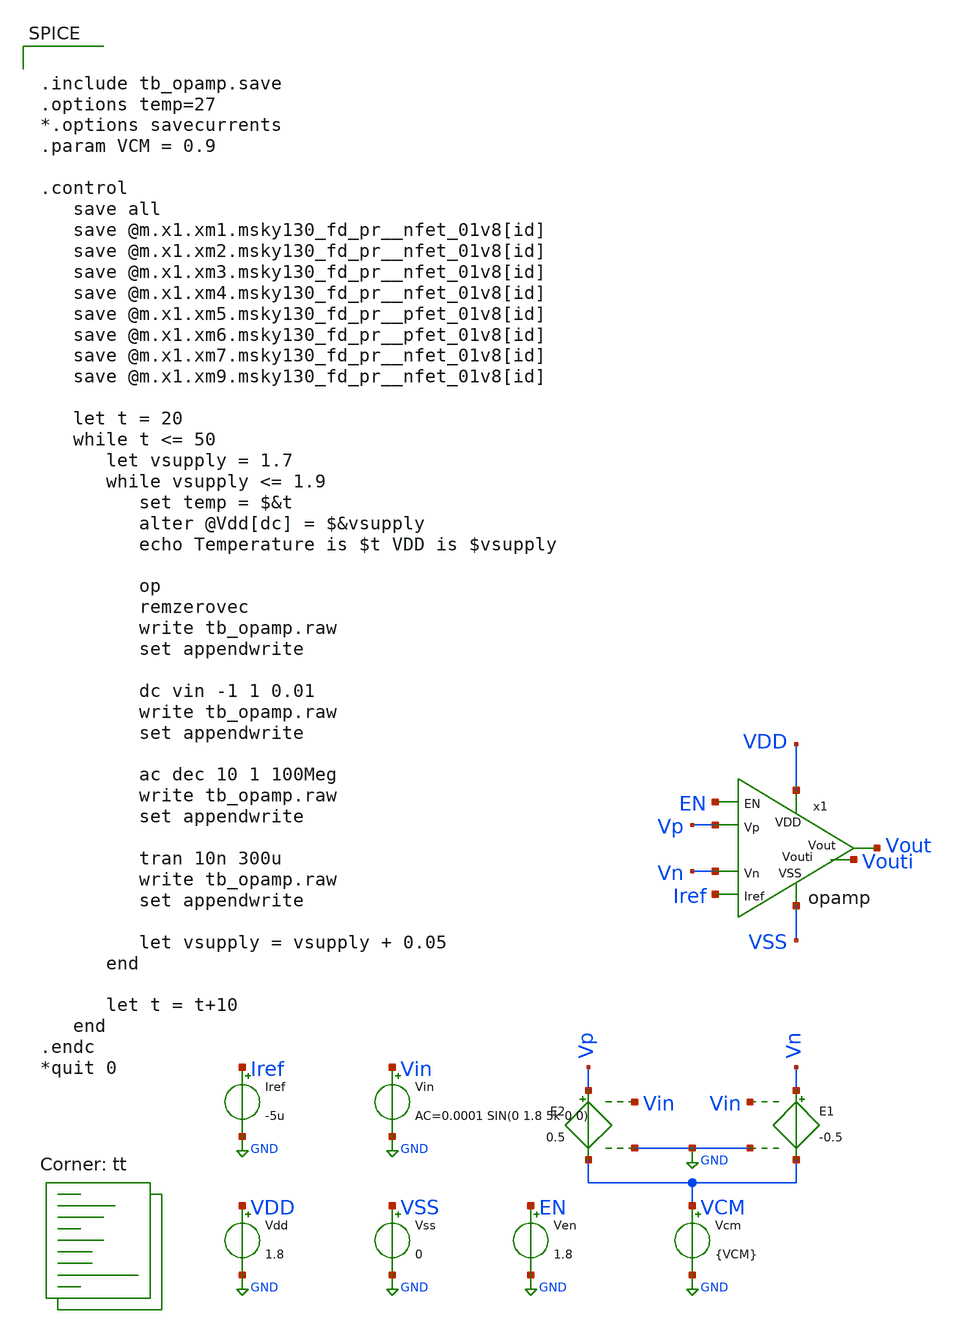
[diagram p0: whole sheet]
** sch_path: xschem/tb_opamp.sch
**.subckt tb_opamp
Vdd VDD GND 1.8
Vss VSS GND 0
E1 Vn VCM Vin GND -0.5
Vcm VCM GND {VCM}
E2 Vp VCM Vin GND 0.5
Vin Vin GND AC=0.0001 SIN(0 1.8 5k 0 0)
Iref Iref GND -5u
x1 Vout Vn Vp VSS Iref VDD Vouti EN opamp
Ven EN GND 1.8
**** begin user architecture code


.include tb_opamp.save
.options temp=27
*.options savecurrents
.param VCM = 0.9

.control
   save all
   save @m.x1.xm1.msky130_fd_pr__nfet_01v8[id]
   save @m.x1.xm2.msky130_fd_pr__nfet_01v8[id]
   save @m.x1.xm3.msky130_fd_pr__nfet_01v8[id]
   save @m.x1.xm4.msky130_fd_pr__nfet_01v8[id]
   save @m.x1.xm5.msky130_fd_pr__pfet_01v8[id]
   save @m.x1.xm6.msky130_fd_pr__pfet_01v8[id]
   save @m.x1.xm7.msky130_fd_pr__nfet_01v8[id]
   save @m.x1.xm9.msky130_fd_pr__nfet_01v8[id]

   let t = 20
   while t <= 50
      let vsupply = 1.7
      while vsupply <= 1.9
         set temp = $&t
         alter @Vdd[dc] = $&vsupply
         echo Temperature is $t VDD is $vsupply

         op
         remzerovec
         write tb_opamp.raw
         set appendwrite

         dc vin -1 1 0.01
         write tb_opamp.raw
         set appendwrite

         ac dec 10 1 100Meg
         write tb_opamp.raw
         set appendwrite

         tran 10n 300u
         write tb_opamp.raw
         set appendwrite

         let vsupply = vsupply + 0.05
      end

      let t = t+10
   end
.endc
*quit 0


.lib $::SKYWATER_MODELS/sky130.lib.spice tt
**** end user architecture code
**.ends

* expanding   symbol:  /foss/designs/ttsky_opamp/xschem/opamp.sym # of pins=8
** sym_path: xschem/opamp.sym
** sch_path: xschem/opamp.sch
.subckt opamp Vout Vn Vp VSS Iref VDD Vouti EN
*.ipin VSS
*.ipin Vp
*.opin Vout
*.ipin Vn
*.ipin VDD
*.ipin Iref
*.opin Vouti
*.ipin EN
XM1 VGref VGref VSS VSS sky130_fd_pr__nfet_01v8 L=1 W=4 nf=1 ad='int((1 + 1)/2) * 4 / 1 * 0.29' as='int((1 + 2)/2) * 4 / 1 * 0.29'
+ pd='2*int((1 + 1)/2) * (4 / 1 + 0.29)' ps='2*int((1 + 2)/2) * (4 / 1 + 0.29)' nrd='0.29 / 4 ' nrs='0.29 / 4 '
+ sa=0 sb=0 sd=0 mult=1 m=1
XM2 Vx VGref VSS VSS sky130_fd_pr__nfet_01v8 L=1 W=4 nf=1 ad='int((1 + 1)/2) * 4 / 1 * 0.29' as='int((1 + 2)/2) * 4 / 1 * 0.29'
+ pd='2*int((1 + 1)/2) * (4 / 1 + 0.29)' ps='2*int((1 + 2)/2) * (4 / 1 + 0.29)' nrd='0.29 / 4 ' nrs='0.29 / 4 '
+ sa=0 sb=0 sd=0 mult=1 m=1
XM3 Vouti Vp Vx VSS sky130_fd_pr__nfet_01v8 L=2 W=2.5 nf=1 ad='int((1 + 1)/2) * 2.5 / 1 * 0.29' as='int((1 + 2)/2) * 2.5 / 1 * 0.29'
+ pd='2*int((1 + 1)/2) * (2.5 / 1 + 0.29)' ps='2*int((1 + 2)/2) * (2.5 / 1 + 0.29)' nrd='0.29 / 2.5 ' nrs='0.29 / 2.5 '
+ sa=0 sb=0 sd=0 mult=1 m=1
XM4 Vg1 Vn Vx VSS sky130_fd_pr__nfet_01v8 L=2 W=2.5 nf=1 ad='int((1 + 1)/2) * 2.5 / 1 * 0.29' as='int((1 + 2)/2) * 2.5 / 1 * 0.29'
+ pd='2*int((1 + 1)/2) * (2.5 / 1 + 0.29)' ps='2*int((1 + 2)/2) * (2.5 / 1 + 0.29)' nrd='0.29 / 2.5 ' nrs='0.29 / 2.5 '
+ sa=0 sb=0 sd=0 mult=1 m=1
XM5 Vouti Vg1 VDD VDD sky130_fd_pr__pfet_01v8 L=2 W=2 nf=1 ad='int((1 + 1)/2) * 2 / 1 * 0.29' as='int((1 + 2)/2) * 2 / 1 * 0.29'
+ pd='2*int((1 + 1)/2) * (2 / 1 + 0.29)' ps='2*int((1 + 2)/2) * (2 / 1 + 0.29)' nrd='0.29 / 2 ' nrs='0.29 / 2 '
+ sa=0 sb=0 sd=0 mult=1 m=1
XM6 Vg1 Vg1 VDD VDD sky130_fd_pr__pfet_01v8 L=2 W=2 nf=1 ad='int((1 + 1)/2) * 2 / 1 * 0.29' as='int((1 + 2)/2) * 2 / 1 * 0.29'
+ pd='2*int((1 + 1)/2) * (2 / 1 + 0.29)' ps='2*int((1 + 2)/2) * (2 / 1 + 0.29)' nrd='0.29 / 2 ' nrs='0.29 / 2 '
+ sa=0 sb=0 sd=0 mult=1 m=1
XM7 Vout VGref VSS VSS sky130_fd_pr__nfet_01v8 L=1 W=32 nf=8 ad='int((8 + 1)/2) * 32 / 8 * 0.29' as='int((8 + 2)/2) * 32 / 8 * 0.29'
+ pd='2*int((8 + 1)/2) * (32 / 8 + 0.29)' ps='2*int((8 + 2)/2) * (32 / 8 + 0.29)' nrd='0.29 / 32 ' nrs='0.29 / 32 '
+ sa=0 sb=0 sd=0 mult=1 m=1
XM8 Vout Vouti VDD VDD sky130_fd_pr__pfet_01v8 L=1 W=20 nf=2 ad='int((2 + 1)/2) * 20 / 2 * 0.29' as='int((2 + 2)/2) * 20 / 2 * 0.29'
+ pd='2*int((2 + 1)/2) * (20 / 2 + 0.29)' ps='2*int((2 + 2)/2) * (20 / 2 + 0.29)' nrd='0.29 / 20 ' nrs='0.29 / 20 '
+ sa=0 sb=0 sd=0 mult=1 m=1
R1 Vout net1 10k m=1
XM9 Iref EN VGref VSS sky130_fd_pr__nfet_01v8 L=2 W=2 nf=1 ad='int((1 + 1)/2) * 2 / 1 * 0.29' as='int((1 + 2)/2) * 2 / 1 * 0.29'
+ pd='2*int((1 + 1)/2) * (2 / 1 + 0.29)' ps='2*int((1 + 2)/2) * (2 / 1 + 0.29)' nrd='0.29 / 2 ' nrs='0.29 / 2 '
+ sa=0 sb=0 sd=0 mult=1 m=1
XC3 Vout GND sky130_fd_pr__cap_mim_m3_1 W=113 L=111 MF=1 m=1
XC1 Vouti net1 sky130_fd_pr__cap_mim_m3_1 W=40 L=50 MF=1 m=1
.ends

.GLOBAL GND
.GLOBAL VDD
.end
